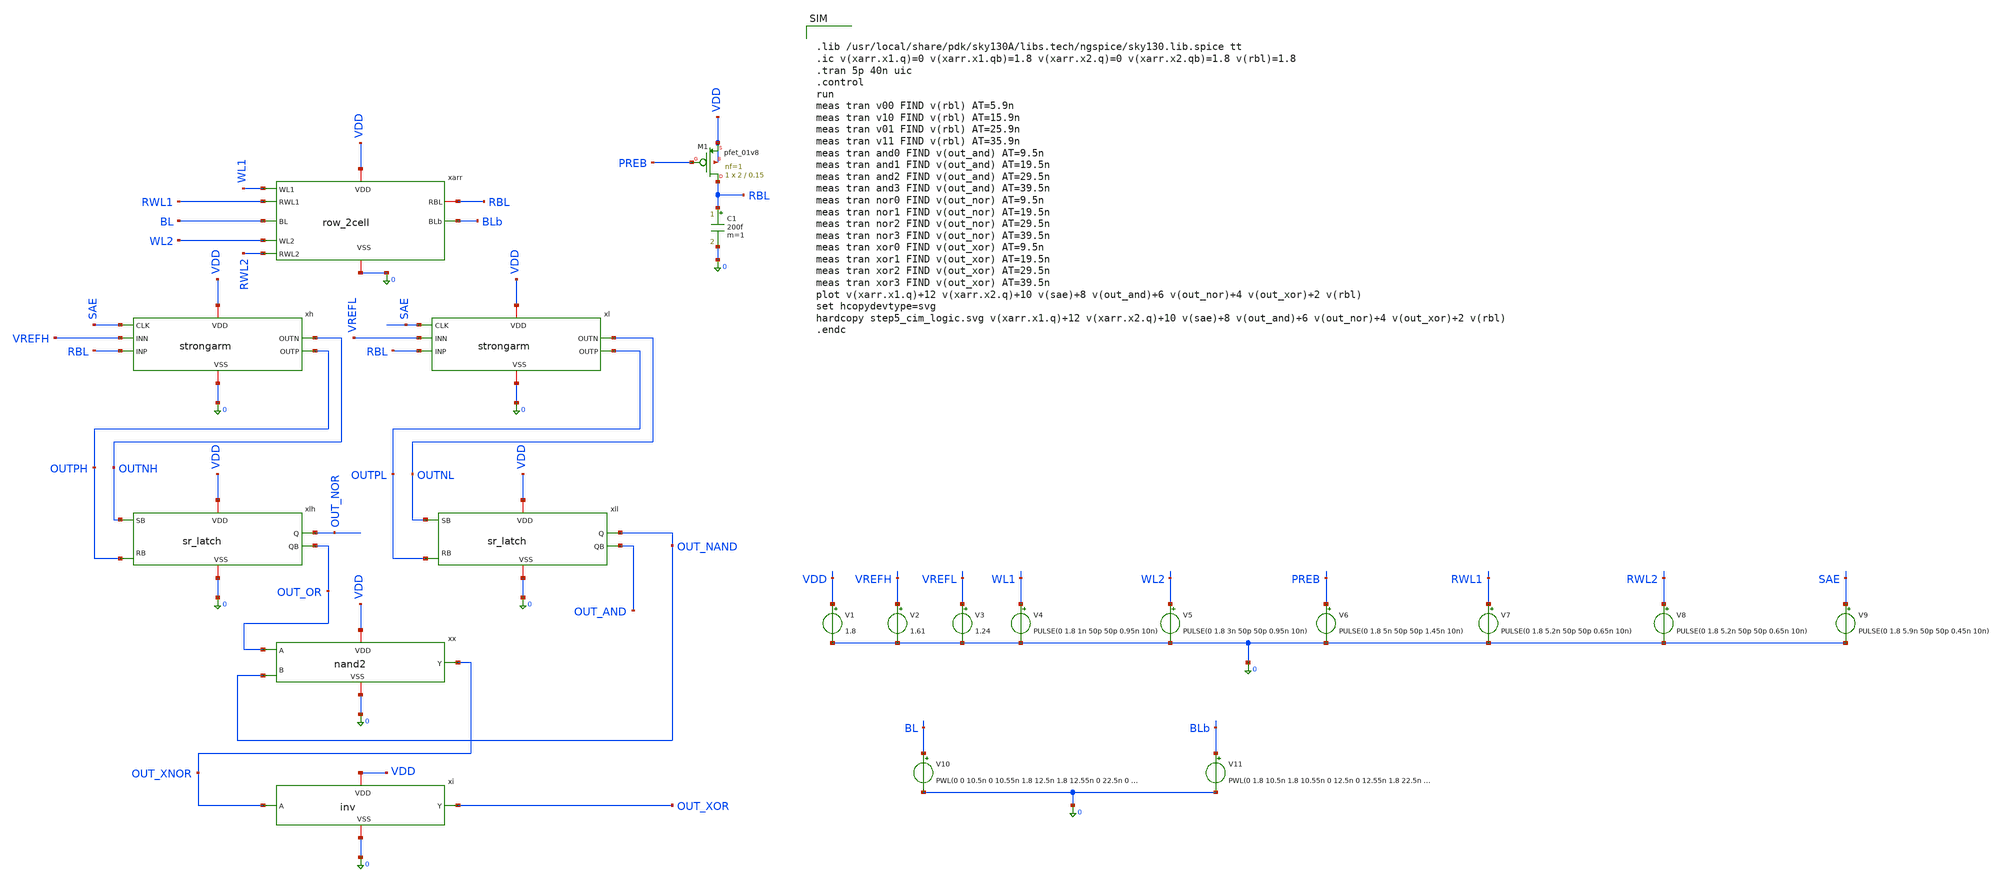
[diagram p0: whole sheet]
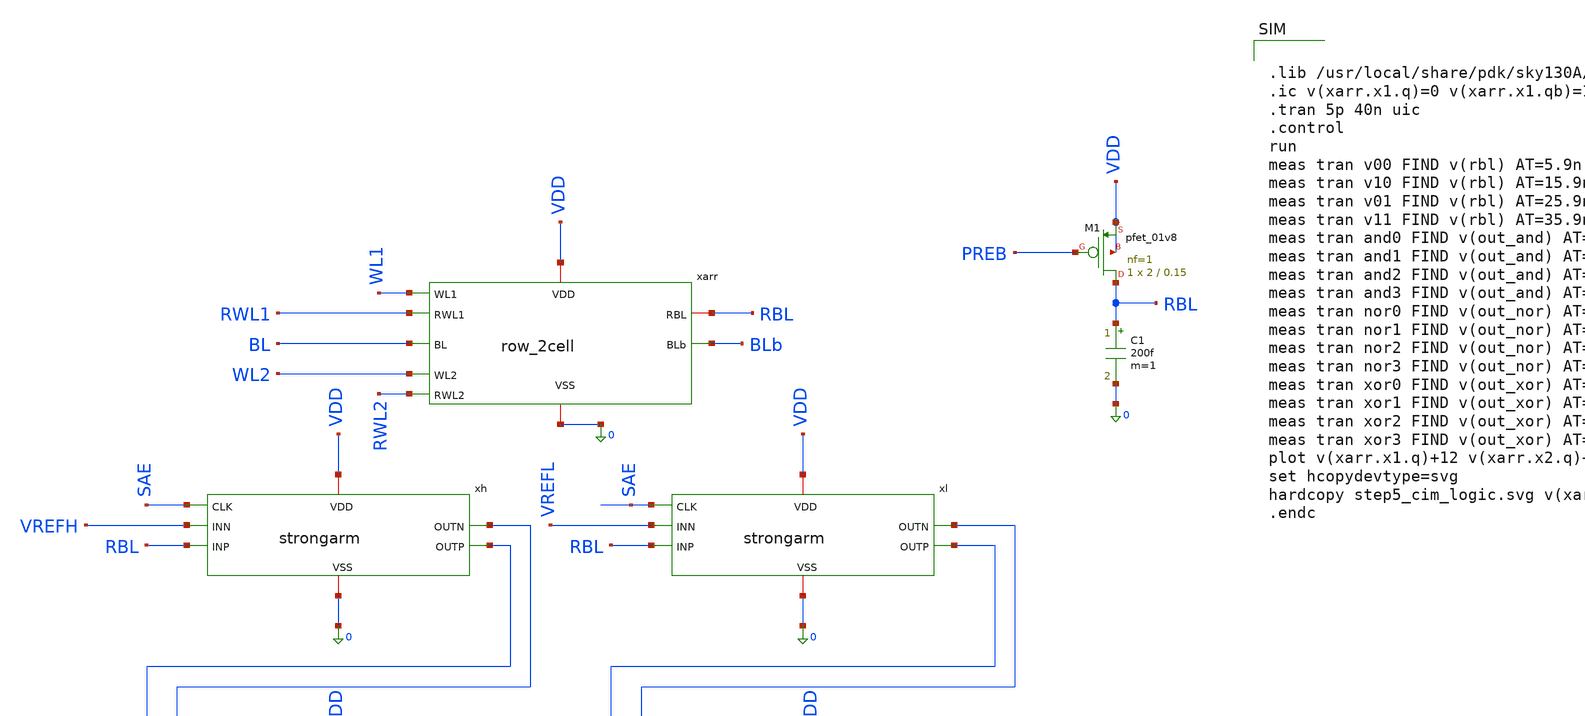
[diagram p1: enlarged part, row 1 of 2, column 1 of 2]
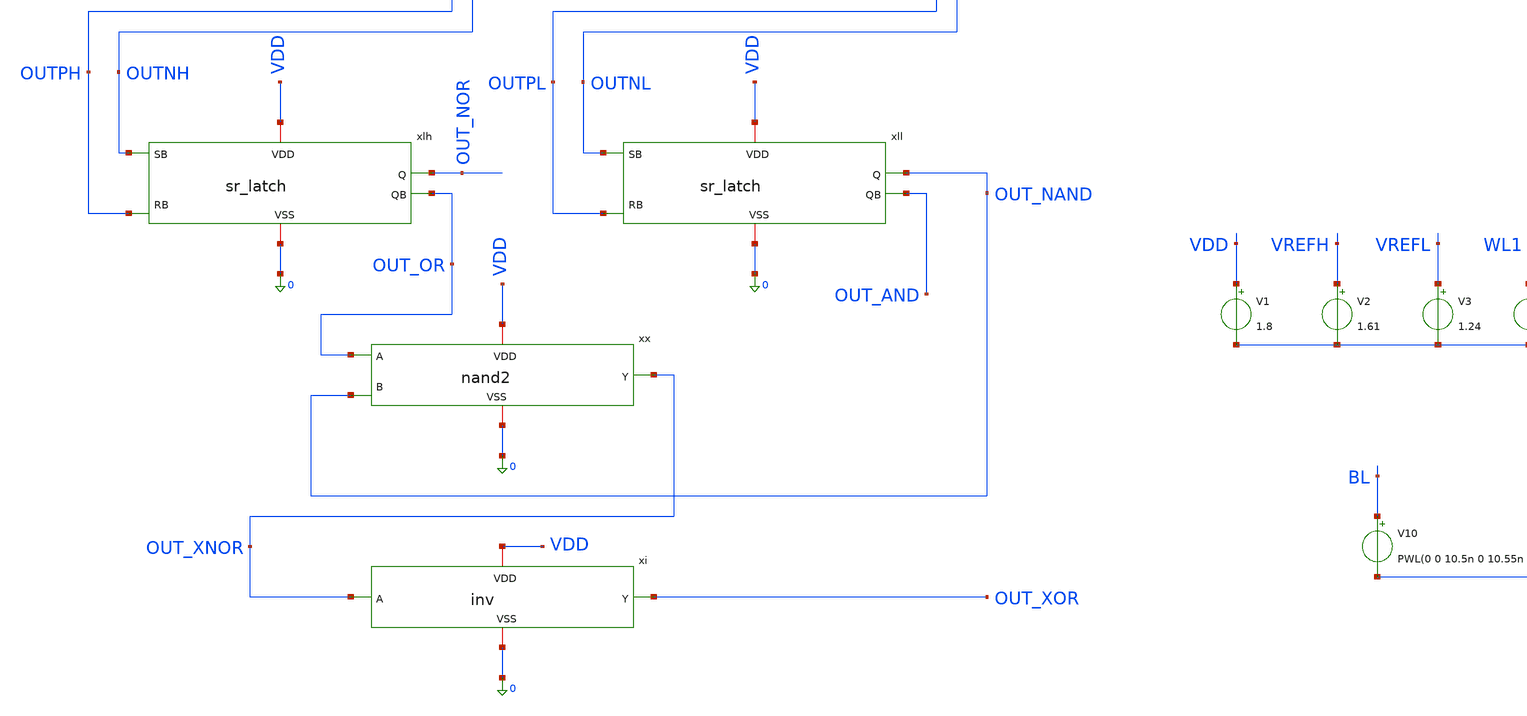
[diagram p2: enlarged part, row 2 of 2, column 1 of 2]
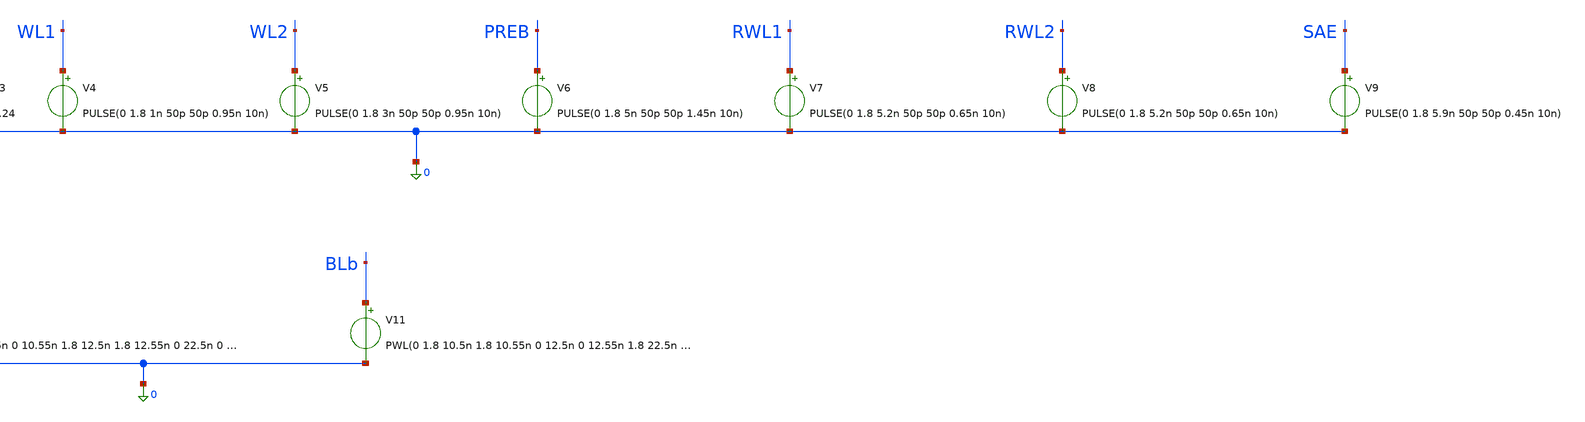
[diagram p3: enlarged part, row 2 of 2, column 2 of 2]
** sch_path: schematics/cim_logic_tb.sch
**.subckt cim_logic_tb
xarr VDD WL1 RWL1 BL BLb WL2 RWL2 RBL 0 row_2cell
xh VDD SAE OUTNH OUTPH VREFH RBL 0 strongarm
xl VDD SAE OUTNL OUTPL VREFL RBL 0 strongarm
xlh VDD OUTNH OUT_NOR OUT_OR OUTPH 0 sr_latch
xll VDD OUTNL OUT_NAND OUT_AND OUTPL 0 sr_latch
xx VDD OUT_OR OUT_XNOR OUT_NAND 0 nand2
xi VDD OUT_XNOR OUT_XOR 0 inv
XM1 RBL PREB VDD VDD sky130_fd_pr__pfet_01v8 L=0.15 W=2 nf=1 ad='int((1 + 1)/2) * 2 / 1 * 0.29' as='int((1 + 2)/2) * 2 / 1 * 0.29'
+ pd='2*int((1 + 1)/2) * (2 / 1 + 0.29)' ps='2*int((1 + 2)/2) * (2 / 1 + 0.29)' nrd='0.29 / 2 ' nrs='0.29 / 2 '
+ sa=0 sb=0 sd=0 mult=1 m=1
C1 RBL 0 200f m=1
V1 VDD 0 1.8
V2 VREFH 0 1.61
V3 VREFL 0 1.24
V4 WL1 0 PULSE(0 1.8 1n 50p 50p 0.95n 10n)
V5 WL2 0 PULSE(0 1.8 3n 50p 50p 0.95n 10n)
V6 PREB 0 PULSE(0 1.8 5n 50p 50p 1.45n 10n)
V7 RWL1 0 PULSE(0 1.8 5.2n 50p 50p 0.65n 10n)
V8 RWL2 0 PULSE(0 1.8 5.2n 50p 50p 0.65n 10n)
V9 SAE 0 PULSE(0 1.8 5.9n 50p 50p 0.45n 10n)
V10 BL 0 PWL(0 0 10.5n 0 10.55n 1.8 12.5n 1.8 12.55n 0 22.5n 0 22.55n 1.8 40n 1.8)
V11 BLb 0 PWL(0 1.8 10.5n 1.8 10.55n 0 12.5n 0 12.55n 1.8 22.5n 1.8 22.55n 0 40n 0)
**** begin user architecture code


.lib /usr/local/share/pdk/sky130A/libs.tech/ngspice/sky130.lib.spice tt
.ic v(xarr.x1.q)=0 v(xarr.x1.qb)=1.8 v(xarr.x2.q)=0 v(xarr.x2.qb)=1.8 v(rbl)=1.8
.tran 5p 40n uic
.control
run
meas tran v00 FIND v(rbl) AT=5.9n
meas tran v10 FIND v(rbl) AT=15.9n
meas tran v01 FIND v(rbl) AT=25.9n
meas tran v11 FIND v(rbl) AT=35.9n
meas tran and0 FIND v(out_and) AT=9.5n
meas tran and1 FIND v(out_and) AT=19.5n
meas tran and2 FIND v(out_and) AT=29.5n
meas tran and3 FIND v(out_and) AT=39.5n
meas tran nor0 FIND v(out_nor) AT=9.5n
meas tran nor1 FIND v(out_nor) AT=19.5n
meas tran nor2 FIND v(out_nor) AT=29.5n
meas tran nor3 FIND v(out_nor) AT=39.5n
meas tran xor0 FIND v(out_xor) AT=9.5n
meas tran xor1 FIND v(out_xor) AT=19.5n
meas tran xor2 FIND v(out_xor) AT=29.5n
meas tran xor3 FIND v(out_xor) AT=39.5n
plot v(xarr.x1.q)+12 v(xarr.x2.q)+10 v(sae)+8 v(out_and)+6 v(out_nor)+4 v(out_xor)+2 v(rbl)
set hcopydevtype=svg
hardcopy step5_cim_logic.svg v(xarr.x1.q)+12 v(xarr.x2.q)+10 v(sae)+8 v(out_and)+6 v(out_nor)+4
+ v(out_xor)+2 v(rbl)
.endc


**** end user architecture code
**.ends
.end
